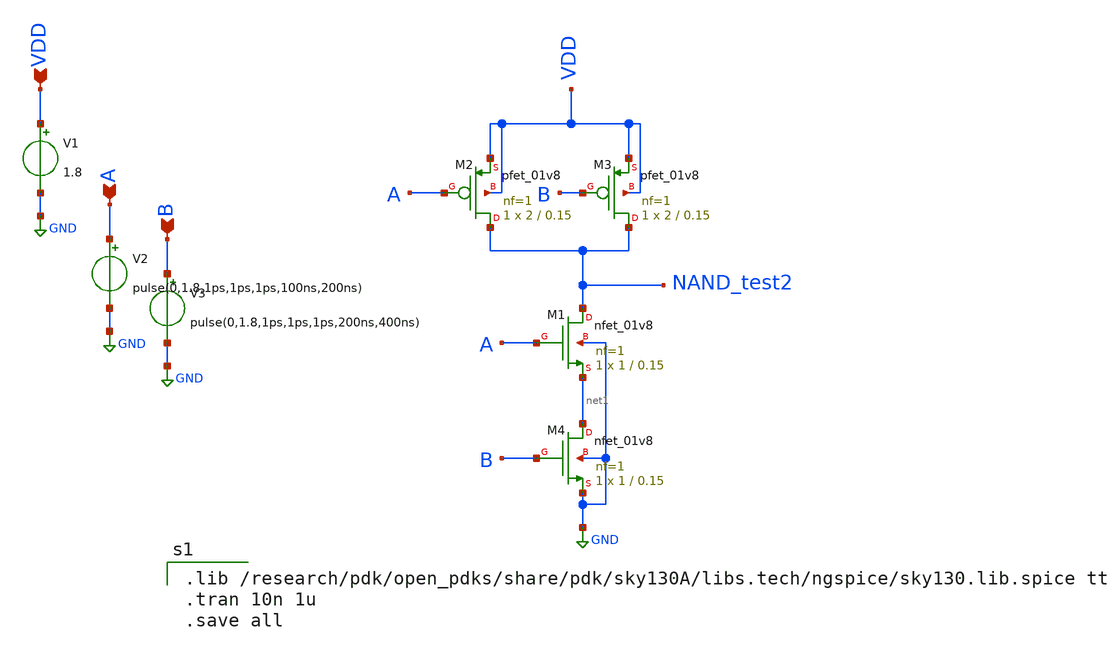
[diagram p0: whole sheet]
** sch_path: skywater_stuff/NAND_test2.sch
**.subckt NAND_test2 VDD A B
*.ipin VDD
*.ipin A
*.ipin B
XM1 NAND_test2 A net1 GND sky130_fd_pr__nfet_01v8 L=0.15 W=1 nf=1 ad='int((nf+1)/2) * W/nf * 0.29' as='int((nf+2)/2) * W/nf * 0.29'
+ pd='2*int((nf+1)/2) * (W/nf + 0.29)' ps='2*int((nf+2)/2) * (W/nf + 0.29)' nrd='0.29 / W' nrs='0.29 / W'
+ sa=0 sb=0 sd=0 mult=1 m=1
XM2 NAND_test2 A VDD VDD sky130_fd_pr__pfet_01v8 L=0.15 W=2 nf=1 ad='int((nf+1)/2) * W/nf * 0.29' as='int((nf+2)/2) * W/nf * 0.29'
+ pd='2*int((nf+1)/2) * (W/nf + 0.29)' ps='2*int((nf+2)/2) * (W/nf + 0.29)' nrd='0.29 / W' nrs='0.29 / W'
+ sa=0 sb=0 sd=0 mult=1 m=1
XM3 NAND_test2 B VDD VDD sky130_fd_pr__pfet_01v8 L=0.15 W=2 nf=1 ad='int((nf+1)/2) * W/nf * 0.29' as='int((nf+2)/2) * W/nf * 0.29'
+ pd='2*int((nf+1)/2) * (W/nf + 0.29)' ps='2*int((nf+2)/2) * (W/nf + 0.29)' nrd='0.29 / W' nrs='0.29 / W'
+ sa=0 sb=0 sd=0 mult=1 m=1
XM4 net1 B GND GND sky130_fd_pr__nfet_01v8 L=0.15 W=1 nf=1 ad='int((nf+1)/2) * W/nf * 0.29' as='int((nf+2)/2) * W/nf * 0.29'
+ pd='2*int((nf+1)/2) * (W/nf + 0.29)' ps='2*int((nf+2)/2) * (W/nf + 0.29)' nrd='0.29 / W' nrs='0.29 / W'
+ sa=0 sb=0 sd=0 mult=1 m=1
V1 VDD GND 1.8
V2 A GND pulse(0,1.8,1ps,1ps,1ps,100ns,200ns)
V3 B GND pulse(0,1.8,1ps,1ps,1ps,200ns,400ns)
**** begin user architecture code

.lib /research/pdk/open_pdks/share/pdk/sky130A/libs.tech/ngspice/sky130.lib.spice tt
.tran 10n 1u
.save all

**** end user architecture code
**.ends
.GLOBAL GND
.end
